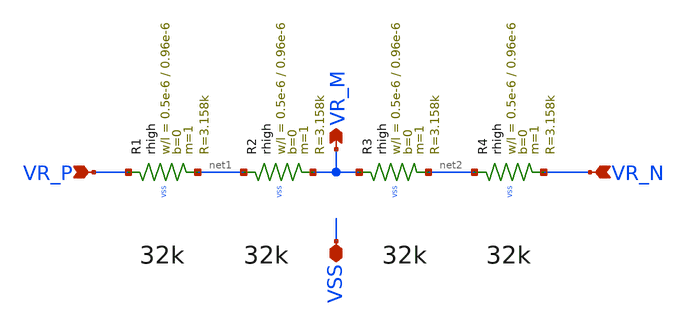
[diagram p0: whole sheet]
** sch_path: macros/filter_cmos5l/schematic/xschem/rstring_cm.sch
**.subckt rstring_cm VSS VR_P VR_N VR_M
*.iopin VSS
*.ipin VR_P
*.ipin VR_N
*.opin VR_M
XR1 VR_P net1 VSS rhigh w=0.5e-6 l=0.96e-6 m=1 b=0 mm_ok=1
XR2 net1 VR_M VSS rhigh w=0.5e-6 l=0.96e-6 m=1 b=0 mm_ok=1
XR3 VR_M net2 VSS rhigh w=0.5e-6 l=0.96e-6 m=1 b=0 mm_ok=1
XR4 net2 VR_N VSS rhigh w=0.5e-6 l=0.96e-6 m=1 b=0 mm_ok=1
**.ends
.end
